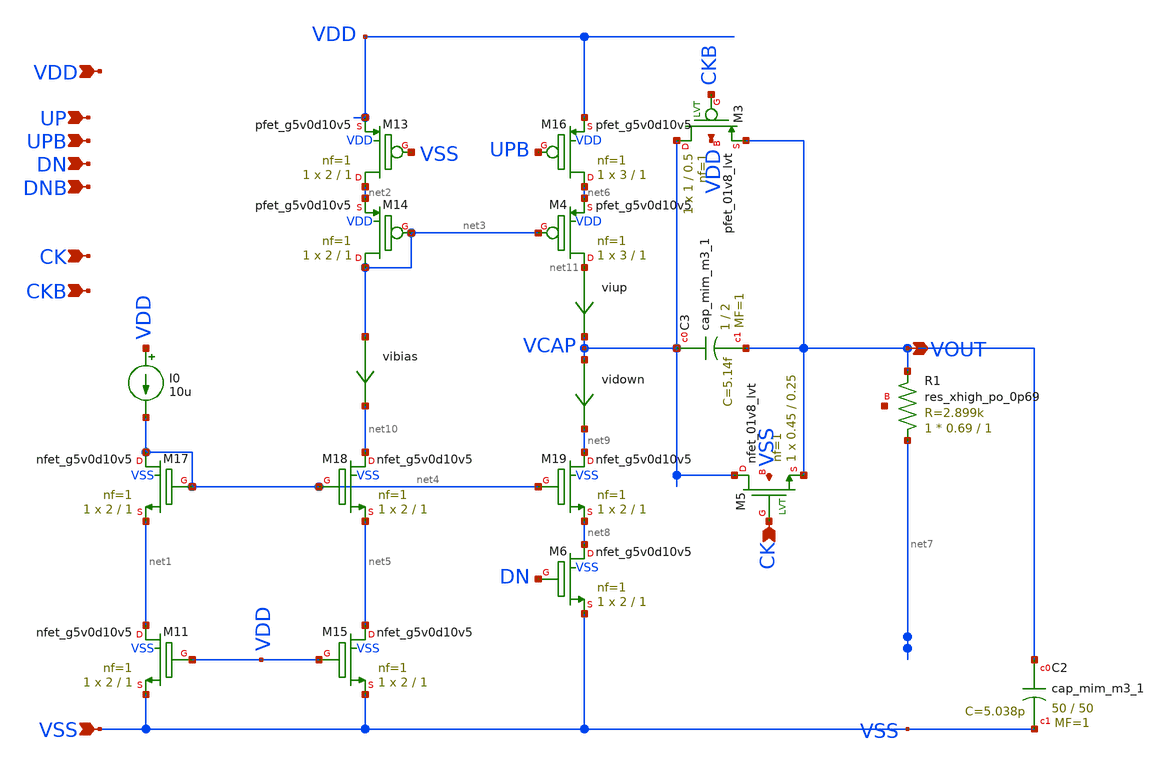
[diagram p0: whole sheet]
** sch_path: xschem/pll_cp_delta_hv.sch
**.subckt pll_cp_delta_hv VOUT VSS UP DNB CK CKB VDD DN UPB CK
*.opin VOUT
*.ipin VSS
*.ipin UP
*.ipin DNB
*.ipin CK
*.ipin CKB
*.ipin VDD
*.ipin DN
*.ipin UPB
*.ipin CK
vibias net3 net10 0
.save i(vibias)
XM16 net6 UPB VDD VDD sky130_fd_pr__pfet_g5v0d10v5 L=1 W=3 nf=1 ad='int((nf+1)/2) * W/nf * 0.29' as='int((nf+2)/2) * W/nf * 0.29'
+ pd='2*int((nf+1)/2) * (W/nf + 0.29)' ps='2*int((nf+2)/2) * (W/nf + 0.29)' nrd='0.29 / W' nrs='0.29 / W'
+ sa=0 sb=0 sd=0 mult=1 m=1
XM13 net2 VSS VDD VDD sky130_fd_pr__pfet_g5v0d10v5 L=1 W=2 nf=1 ad='int((nf+1)/2) * W/nf * 0.29' as='int((nf+2)/2) * W/nf * 0.29'
+ pd='2*int((nf+1)/2) * (W/nf + 0.29)' ps='2*int((nf+2)/2) * (W/nf + 0.29)' nrd='0.29 / W' nrs='0.29 / W'
+ sa=0 sb=0 sd=0 mult=1 m=1
XM14 net3 net3 net2 VDD sky130_fd_pr__pfet_g5v0d10v5 L=1 W=2 nf=1 ad='int((nf+1)/2) * W/nf * 0.29' as='int((nf+2)/2) * W/nf * 0.29'
+ pd='2*int((nf+1)/2) * (W/nf + 0.29)' ps='2*int((nf+2)/2) * (W/nf + 0.29)' nrd='0.29 / W' nrs='0.29 / W'
+ sa=0 sb=0 sd=0 mult=1 m=1
I0 VDD net4 10u
XM11 net1 VDD VSS VSS sky130_fd_pr__nfet_g5v0d10v5 L=1 W=2 nf=1 ad='int((nf+1)/2) * W/nf * 0.29' as='int((nf+2)/2) * W/nf * 0.29'
+ pd='2*int((nf+1)/2) * (W/nf + 0.29)' ps='2*int((nf+2)/2) * (W/nf + 0.29)' nrd='0.29 / W' nrs='0.29 / W'
+ sa=0 sb=0 sd=0 mult=1 m=1
XM17 net4 net4 net1 VSS sky130_fd_pr__nfet_g5v0d10v5 L=1 W=2 nf=1 ad='int((nf+1)/2) * W/nf * 0.29' as='int((nf+2)/2) * W/nf * 0.29'
+ pd='2*int((nf+1)/2) * (W/nf + 0.29)' ps='2*int((nf+2)/2) * (W/nf + 0.29)' nrd='0.29 / W' nrs='0.29 / W'
+ sa=0 sb=0 sd=0 mult=1 m=1
XM15 net5 VDD VSS VSS sky130_fd_pr__nfet_g5v0d10v5 L=1 W=2 nf=1 ad='int((nf+1)/2) * W/nf * 0.29' as='int((nf+2)/2) * W/nf * 0.29'
+ pd='2*int((nf+1)/2) * (W/nf + 0.29)' ps='2*int((nf+2)/2) * (W/nf + 0.29)' nrd='0.29 / W' nrs='0.29 / W'
+ sa=0 sb=0 sd=0 mult=1 m=1
XM18 net10 net4 net5 VSS sky130_fd_pr__nfet_g5v0d10v5 L=1 W=2 nf=1 ad='int((nf+1)/2) * W/nf * 0.29' as='int((nf+2)/2) * W/nf * 0.29'
+ pd='2*int((nf+1)/2) * (W/nf + 0.29)' ps='2*int((nf+2)/2) * (W/nf + 0.29)' nrd='0.29 / W' nrs='0.29 / W'
+ sa=0 sb=0 sd=0 mult=1 m=1
XM6 net8 DN VSS VSS sky130_fd_pr__nfet_g5v0d10v5 L=1 W=2 nf=1 ad='int((nf+1)/2) * W/nf * 0.29' as='int((nf+2)/2) * W/nf * 0.29'
+ pd='2*int((nf+1)/2) * (W/nf + 0.29)' ps='2*int((nf+2)/2) * (W/nf + 0.29)' nrd='0.29 / W' nrs='0.29 / W'
+ sa=0 sb=0 sd=0 mult=1 m=1
XM19 net9 net4 net8 VSS sky130_fd_pr__nfet_g5v0d10v5 L=1 W=2 nf=1 ad='int((nf+1)/2) * W/nf * 0.29' as='int((nf+2)/2) * W/nf * 0.29'
+ pd='2*int((nf+1)/2) * (W/nf + 0.29)' ps='2*int((nf+2)/2) * (W/nf + 0.29)' nrd='0.29 / W' nrs='0.29 / W'
+ sa=0 sb=0 sd=0 mult=1 m=1
XM4 net11 net3 net6 VDD sky130_fd_pr__pfet_g5v0d10v5 L=1 W=3 nf=1 ad='int((nf+1)/2) * W/nf * 0.29' as='int((nf+2)/2) * W/nf * 0.29'
+ pd='2*int((nf+1)/2) * (W/nf + 0.29)' ps='2*int((nf+2)/2) * (W/nf + 0.29)' nrd='0.29 / W' nrs='0.29 / W'
+ sa=0 sb=0 sd=0 mult=1 m=1
viup net11 VCAP 0
.save i(viup)
vidown VCAP net9 0
.save i(vidown)
XC3 VCAP VOUT sky130_fd_pr__cap_mim_m3_1 W=1 L=2 MF=1 m=1
XM3 VCAP CKB VOUT VDD sky130_fd_pr__pfet_01v8_lvt L=0.5 W=1 nf=1 ad='int((nf+1)/2) * W/nf * 0.29' as='int((nf+2)/2) * W/nf * 0.29'
+ pd='2*int((nf+1)/2) * (W/nf + 0.29)' ps='2*int((nf+2)/2) * (W/nf + 0.29)' nrd='0.29 / W' nrs='0.29 / W'
+ sa=0 sb=0 sd=0 mult=1 m=1
XM5 VCAP CK VOUT VSS sky130_fd_pr__nfet_01v8_lvt L=0.25 W=0.45 nf=1 ad='int((nf+1)/2) * W/nf * 0.29'
+ as='int((nf+2)/2) * W/nf * 0.29' pd='2*int((nf+1)/2) * (W/nf + 0.29)' ps='2*int((nf+2)/2) * (W/nf + 0.29)'
+ nrd='0.29 / W' nrs='0.29 / W' sa=0 sb=0 sd=0 mult=1 m=1
XC2 VOUT VSS sky130_fd_pr__cap_mim_m3_1 W=50 L=50 MF=1 m=1
XR1 net7 VOUT net12 sky130_fd_pr__res_xhigh_po_0p69 L=1 mult=1 m=1
**.ends
.end
